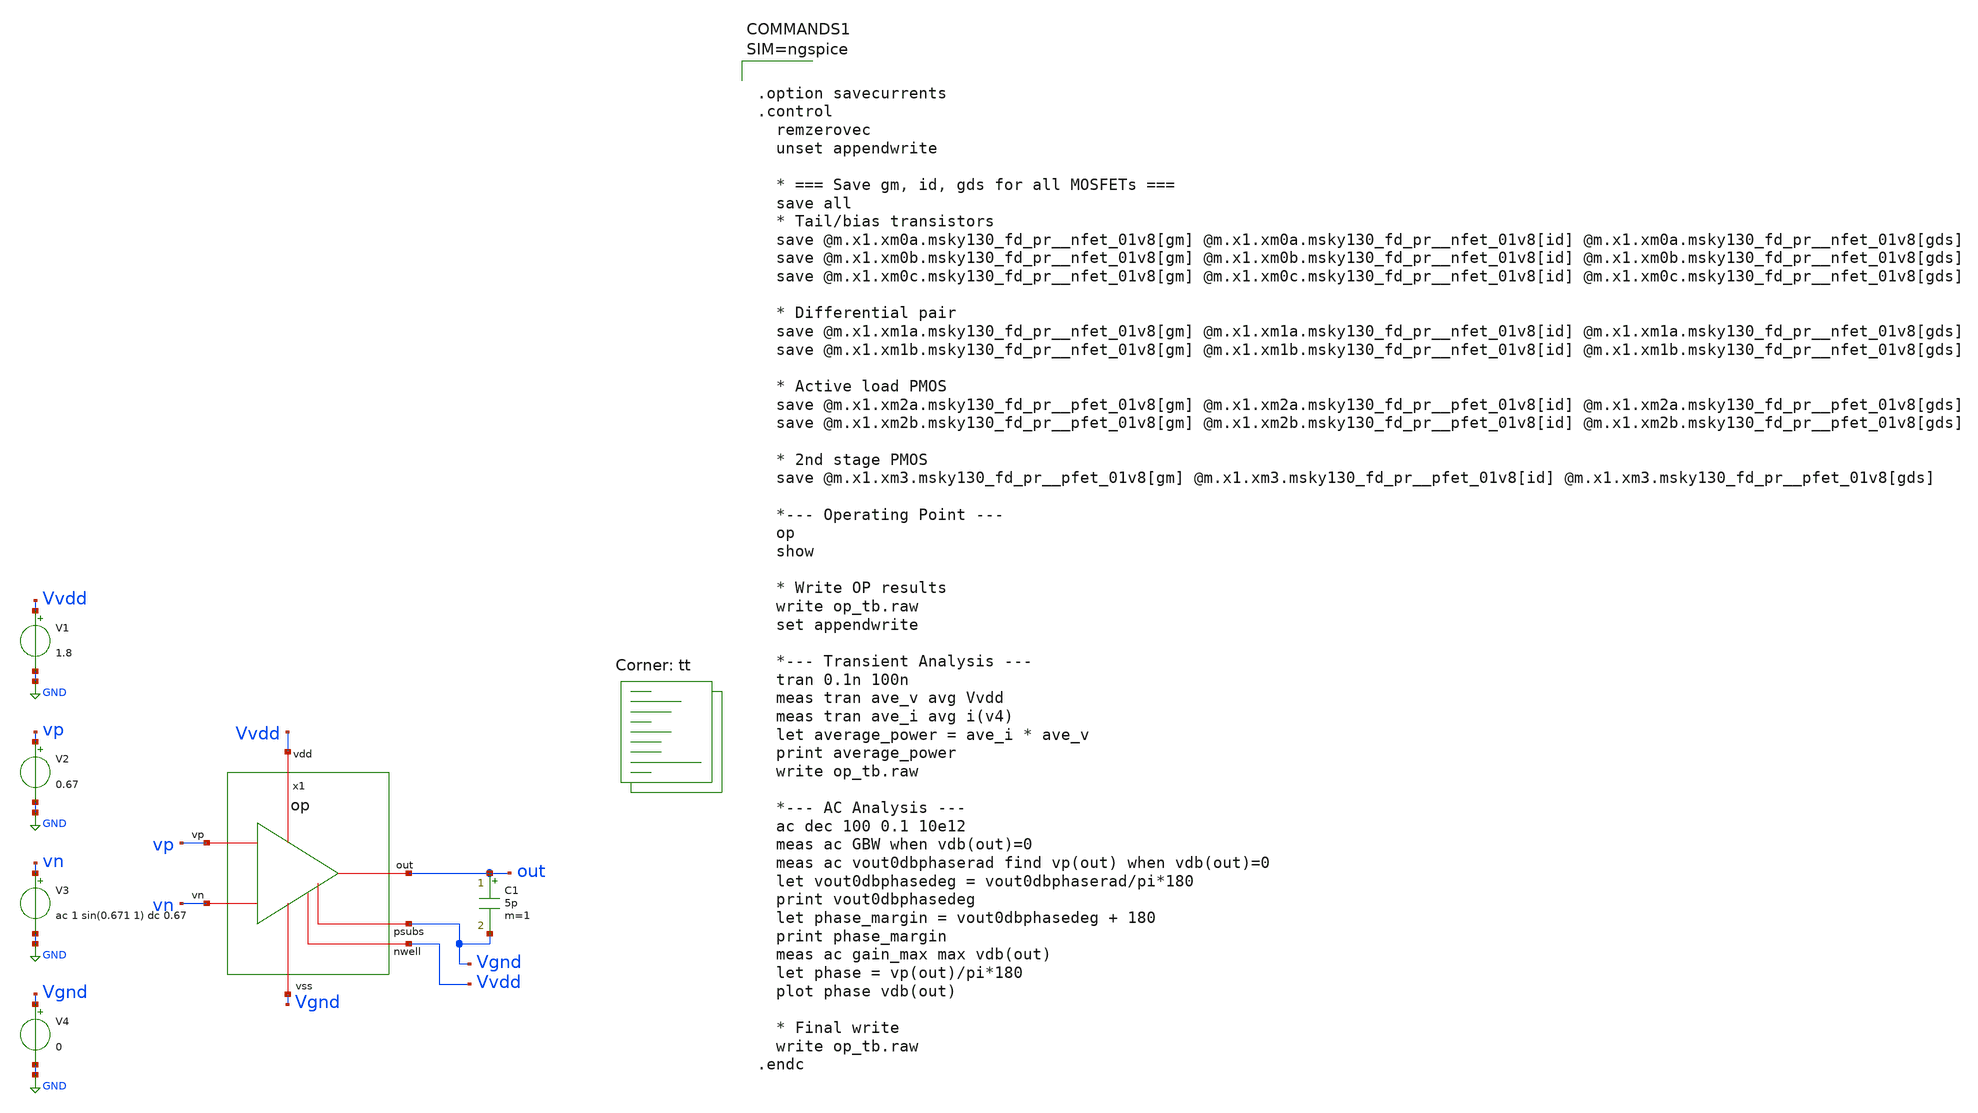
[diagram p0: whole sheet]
** sch_path: xschem/op_tb.sch
**.subckt op_tb
V1 Vvdd GND 1.8
V2 vp GND 0.67
V3 vn GND ac 1 sin(0.671 1) dc 0.67
x1 out Vvdd Vgnd vp vn Vgnd Vvdd op
V4 Vgnd GND 0
C1 out Vgnd 5p m=1
**** begin user architecture code



.option savecurrents
.control
  remzerovec
  unset appendwrite

  * === Save gm, id, gds for all MOSFETs ===
  save all
  * Tail/bias transistors
  save @m.x1.xm0a.msky130_fd_pr__nfet_01v8[gm] @m.x1.xm0a.msky130_fd_pr__nfet_01v8[id]
+ @m.x1.xm0a.msky130_fd_pr__nfet_01v8[gds]
  save @m.x1.xm0b.msky130_fd_pr__nfet_01v8[gm] @m.x1.xm0b.msky130_fd_pr__nfet_01v8[id]
+ @m.x1.xm0b.msky130_fd_pr__nfet_01v8[gds]
  save @m.x1.xm0c.msky130_fd_pr__nfet_01v8[gm] @m.x1.xm0c.msky130_fd_pr__nfet_01v8[id]
+ @m.x1.xm0c.msky130_fd_pr__nfet_01v8[gds]

  * Differential pair
  save @m.x1.xm1a.msky130_fd_pr__nfet_01v8[gm] @m.x1.xm1a.msky130_fd_pr__nfet_01v8[id]
+ @m.x1.xm1a.msky130_fd_pr__nfet_01v8[gds]
  save @m.x1.xm1b.msky130_fd_pr__nfet_01v8[gm] @m.x1.xm1b.msky130_fd_pr__nfet_01v8[id]
+ @m.x1.xm1b.msky130_fd_pr__nfet_01v8[gds]

  * Active load PMOS
  save @m.x1.xm2a.msky130_fd_pr__pfet_01v8[gm] @m.x1.xm2a.msky130_fd_pr__pfet_01v8[id]
+ @m.x1.xm2a.msky130_fd_pr__pfet_01v8[gds]
  save @m.x1.xm2b.msky130_fd_pr__pfet_01v8[gm] @m.x1.xm2b.msky130_fd_pr__pfet_01v8[id]
+ @m.x1.xm2b.msky130_fd_pr__pfet_01v8[gds]

  * 2nd stage PMOS
  save @m.x1.xm3.msky130_fd_pr__pfet_01v8[gm] @m.x1.xm3.msky130_fd_pr__pfet_01v8[id]
+ @m.x1.xm3.msky130_fd_pr__pfet_01v8[gds]

  *--- Operating Point ---
  op
  show

  * Write OP results
  write op_tb.raw
  set appendwrite

  *--- Transient Analysis ---
  tran 0.1n 100n
  meas tran ave_v avg Vvdd
  meas tran ave_i avg i(v4)
  let average_power = ave_i * ave_v
  print average_power
  write op_tb.raw

  *--- AC Analysis ---
  ac dec 100 0.1 10e12
  meas ac GBW when vdb(out)=0
  meas ac vout0dbphaserad find vp(out) when vdb(out)=0
  let vout0dbphasedeg = vout0dbphaserad/pi*180
  print vout0dbphasedeg
  let phase_margin = vout0dbphasedeg + 180
  print phase_margin
  meas ac gain_max max vdb(out)
  let phase = vp(out)/pi*180
  plot phase vdb(out)

  * Final write
  write op_tb.raw
.endc




.lib $::SKYWATER_MODELS/sky130.lib.spice tt
**** end user architecture code
**.ends

* expanding   symbol:  op.sym # of pins=7
** sym_path: xschem/op.sym
** sch_path: xschem/op.sch
.subckt op out vdd vss vp vn psubs nwell
*.iopin vss
*.iopin vdd
*.opin out
*.ipin vp
*.ipin vn
*.iopin psubs
*.iopin nwell
XM3 out net1 vdd nwell sky130_fd_pr__pfet_01v8 L={l3} W={w3} nf={nf3} ad='int((nf+1)/2) * W/nf * 0.29'
+ as='int((nf+2)/2) * W/nf * 0.29' pd='2*int((nf+1)/2) * (W/nf + 0.29)' ps='2*int((nf+2)/2) * (W/nf + 0.29)'
+ nrd='0.29 / W' nrs='0.29 / W' sa=0 sb=0 sd=0 mult=1 m=1
XM1b net1 vn net2 psubs sky130_fd_pr__nfet_01v8 L={l1} W={w1} nf={nf1} ad='int((nf+1)/2) * W/nf * 0.29'
+ as='int((nf+2)/2) * W/nf * 0.29' pd='2*int((nf+1)/2) * (W/nf + 0.29)' ps='2*int((nf+2)/2) * (W/nf + 0.29)'
+ nrd='0.29 / W' nrs='0.29 / W' sa=0 sb=0 sd=0 mult=1 m=1
XM1a net3 vp net2 psubs sky130_fd_pr__nfet_01v8 L={l1} W={w1} nf={nf1} ad='int((nf+1)/2) * W/nf * 0.29'
+ as='int((nf+2)/2) * W/nf * 0.29' pd='2*int((nf+1)/2) * (W/nf + 0.29)' ps='2*int((nf+2)/2) * (W/nf + 0.29)'
+ nrd='0.29 / W' nrs='0.29 / W' sa=0 sb=0 sd=0 mult=1 m=1
XR1 net4 net1 vss sky130_fd_pr__res_high_po_0p35 L={lrz} mult=1 m=1
XC1 out net4 sky130_fd_pr__cap_mim_m3_1 W={wc} L={wc} MF={mc} m={mc}
**** begin user architecture code


.include ../sizing_opamp.spice


**** end user architecture code
XM2a net3 net3 vdd nwell sky130_fd_pr__pfet_01v8 L={l2} W={w2} nf={nf2} ad='int(({nf2} + 1)/2) * {w2} / {nf2} * 0.29'
+ as='int(({nf2} + 2)/2) * {w2} / {nf2} * 0.29' pd='2*int(({nf2} + 1)/2) * ({w2} / {nf2} + 0.29)' ps='2*int(({nf2} + 2)/2) * ({w2} / {nf2} + 0.29)'
+ nrd='0.29 / {w2} ' nrs='0.29 / {w2} ' sa=0 sb=0 sd=0 mult=1 m=1
XM2b net1 net3 vdd nwell sky130_fd_pr__pfet_01v8 L={l2} W={w2} nf={nf2} ad='int(({nf2} + 1)/2) * {w2} / {nf2} * 0.29'
+ as='int(({nf2} + 2)/2) * {w2} / {nf2} * 0.29' pd='2*int(({nf2} + 1)/2) * ({w2} / {nf2} + 0.29)' ps='2*int(({nf2} + 2)/2) * ({w2} / {nf2} + 0.29)'
+ nrd='0.29 / {w2} ' nrs='0.29 / {w2} ' sa=0 sb=0 sd=0 mult=1 m=1
XM0a bias bias vss psubs sky130_fd_pr__nfet_01v8 L={l0} W={w0} nf={nf0} ad='int(({nf0} + 1)/2) * {w0} / {nf0} * 0.29'
+ as='int(({nf0} + 2)/2) * {w0} / {nf0} * 0.29' pd='2*int(({nf0} + 1)/2) * ({w0} / {nf0} + 0.29)' ps='2*int(({nf0} + 2)/2) * ({w0} / {nf0} + 0.29)'
+ nrd='0.29 / {w0} ' nrs='0.29 / {w0} ' sa=0 sb=0 sd=0 mult=1 m=1
I0 vdd bias {i_tail}
XM0b net2 bias vss psubs sky130_fd_pr__nfet_01v8 L={l0} W={w0} nf={nf0} ad='int(({nf0} + 1)/2) * {w0} / {nf0} * 0.29'
+ as='int(({nf0} + 2)/2) * {w0} / {nf0} * 0.29' pd='2*int(({nf0} + 1)/2) * ({w0} / {nf0} + 0.29)' ps='2*int(({nf0} + 2)/2) * ({w0} / {nf0} + 0.29)'
+ nrd='0.29 / {w0} ' nrs='0.29 / {w0} ' sa=0 sb=0 sd=0 mult=1 m=1
XM0c out bias vss psubs sky130_fd_pr__nfet_01v8 L={l0} W={w0} nf={nf0} ad='int(({nf0} + 1)/2) * {w0} / {nf0} * 0.29'
+ as='int(({nf0} + 2)/2) * {w0} / {nf0} * 0.29' pd='2*int(({nf0} + 1)/2) * ({w0} / {nf0} + 0.29)' ps='2*int(({nf0} + 2)/2) * ({w0} / {nf0} + 0.29)'
+ nrd='0.29 / {w0} ' nrs='0.29 / {w0} ' sa=0 sb=0 sd=0 mult=1 m=1
.ends

.GLOBAL GND
.end
